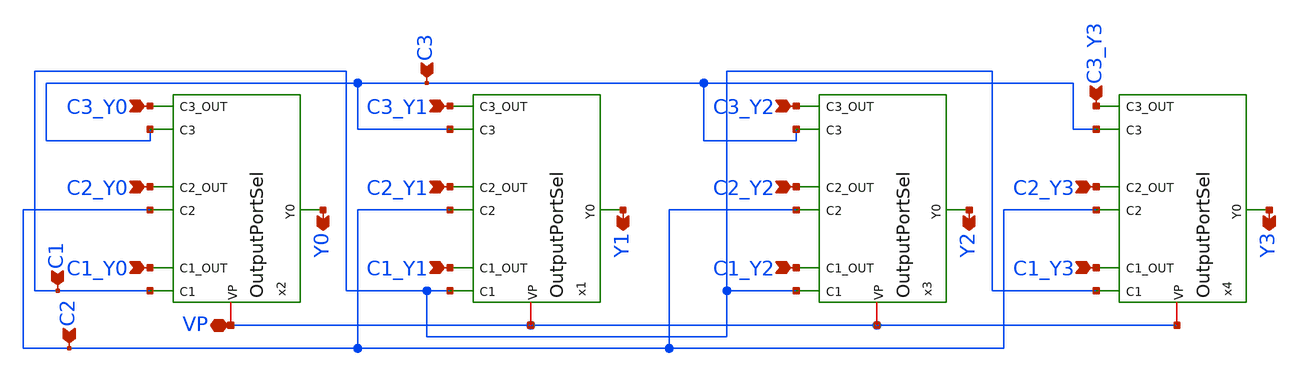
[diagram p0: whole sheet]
** sch_path: ALU_TOP_MODEL/TOPOutSel.sch
**.subckt TOPOutSel C1_Y1 VP Y0 Y1 Y2 Y3 C1_Y2 C1_Y3 C1_Y0 C2_Y0 C2_Y3 C2_Y2 C2_Y1 C3_Y0 C3_Y3 C3_Y2
*+ C3_Y1 C3 C1 C2
*.ipin C1_Y1
*.iopin VP
*.opin Y0
*.opin Y1
*.opin Y2
*.opin Y3
*.ipin C1_Y2
*.ipin C1_Y3
*.ipin C1_Y0
*.ipin C2_Y0
*.ipin C2_Y3
*.ipin C2_Y2
*.ipin C2_Y1
*.ipin C3_Y0
*.ipin C3_Y3
*.ipin C3_Y2
*.ipin C3_Y1
*.ipin C3
*.ipin C1
*.ipin C2
x2 VP C1 C1_Y0 C2 C2_Y0 C3_Y0 Y0 C3 OutputPortSel
x1 VP C1 C1_Y1 C2 C2_Y1 C3_Y1 Y1 C3 OutputPortSel
x3 VP C1 C1_Y2 C2 C2_Y2 C3_Y2 Y2 C3 OutputPortSel
x4 VP C1 C1_Y3 C2 C2_Y3 C3_Y3 Y3 C3 OutputPortSel
**.ends

* expanding   symbol:  OutputPortSel.sym # of pins=8
** sym_path: ALU_TOP_MODEL/OutputPortSel.sym
** sch_path: ALU_TOP_MODEL/OutputPortSel.sch
.subckt OutputPortSel VP C1 C1_OUT C2 C2_OUT C3 Y0 C3_OUT
*.ipin C1
*.ipin C1_OUT
*.ipin C2
*.ipin C2_OUT
*.ipin C3
*.ipin C3_OUT
*.iopin VP
*.opin Y0
x1 net1 C1 C1_OUT VP StaticAndGate
x6 net2 C2 C2_OUT VP StaticAndGate
x7 net4 C3 C3_OUT VP StaticAndGate
x3 net1 net2 net3 VP StaticORGate
x4 net3 net4 Y0 VP StaticORGate
.ends


* expanding   symbol:
*+  /home/safal/projects/GitHub_CMOS_4bit_ALU/AllSymbols&Sch/Gates/StaticAndGate.sym # of pins=4
** sym_path: AllSymbols&Sch/Gates/StaticAndGate.sym
** sch_path: AllSymbols&Sch/Gates/StaticAndGate.sch
.subckt StaticAndGate ANDOUT AND_IN1 AND_IN2 VP
*.ipin AND_IN1
*.opin ANDOUT
*.ipin AND_IN2
*.iopin VP
XM1 net2 AND_IN2 VP VP sky130_fd_pr__pfet_01v8 L=0.15 W=1 nf=1 ad='int((1 + 1)/2) * 1 / 1 * 0.29' as='int((1 + 2)/2) * 1 / 1 * 0.29'
+ pd='2*int((1 + 1)/2) * (1 / 1 + 0.29)' ps='2*int((1 + 2)/2) * (1 / 1 + 0.29)' nrd='0.29 / 1 ' nrs='0.29 / 1 '
+ sa=0 sb=0 sd=0 mult=1 m=1
XM2 net2 AND_IN1 net1 net1 sky130_fd_pr__nfet_01v8 L=0.15 W=2 nf=1 ad='int((1 + 1)/2) * 2 / 1 * 0.29'
+ as='int((1 + 2)/2) * 2 / 1 * 0.29' pd='2*int((1 + 1)/2) * (2 / 1 + 0.29)' ps='2*int((1 + 2)/2) * (2 / 1 + 0.29)'
+ nrd='0.29 / 2 ' nrs='0.29 / 2 ' sa=0 sb=0 sd=0 mult=1 m=1
XM3 net1 AND_IN2 GND GND sky130_fd_pr__nfet_01v8 L=0.15 W=2 nf=1 ad='int((1 + 1)/2) * 2 / 1 * 0.29' as='int((1 + 2)/2) * 2 / 1 * 0.29'
+ pd='2*int((1 + 1)/2) * (2 / 1 + 0.29)' ps='2*int((1 + 2)/2) * (2 / 1 + 0.29)' nrd='0.29 / 2 ' nrs='0.29 / 2 '
+ sa=0 sb=0 sd=0 mult=1 m=1
XM4 net2 AND_IN1 VP VP sky130_fd_pr__pfet_01v8 L=0.15 W=1 nf=1 ad='int((1 + 1)/2) * 1 / 1 * 0.29' as='int((1 + 2)/2) * 1 / 1 * 0.29'
+ pd='2*int((1 + 1)/2) * (1 / 1 + 0.29)' ps='2*int((1 + 2)/2) * (1 / 1 + 0.29)' nrd='0.29 / 1 ' nrs='0.29 / 1 '
+ sa=0 sb=0 sd=0 mult=1 m=1
x1 VP ANDOUT net2 inverter
.ends


* expanding   symbol:
*+  /home/safal/projects/GitHub_CMOS_4bit_ALU/AllSymbols&Sch/Gates/StaticORGate.sym # of pins=4
** sym_path: AllSymbols&Sch/Gates/StaticORGate.sym
** sch_path: AllSymbols&Sch/Gates/StaticORGate.sch
.subckt StaticORGate OR_IN2 OR_IN1 OR_OUT VP
*.ipin OR_IN1
*.opin OR_OUT
*.ipin OR_IN2
*.iopin VP
XM1 net2 OR_IN1 net1 net1 sky130_fd_pr__pfet_01v8 L=0.15 W=8 nf=1 ad='int((1 + 1)/2) * 8 / 1 * 0.29'
+ as='int((1 + 2)/2) * 8 / 1 * 0.29' pd='2*int((1 + 1)/2) * (8 / 1 + 0.29)' ps='2*int((1 + 2)/2) * (8 / 1 + 0.29)'
+ nrd='0.29 / 8 ' nrs='0.29 / 8 ' sa=0 sb=0 sd=0 mult=1 m=1
XM2 net2 OR_IN1 GND GND sky130_fd_pr__nfet_01v8 L=0.15 W=1 nf=1 ad='int((1 + 1)/2) * 1 / 1 * 0.29' as='int((1 + 2)/2) * 1 / 1 * 0.29'
+ pd='2*int((1 + 1)/2) * (1 / 1 + 0.29)' ps='2*int((1 + 2)/2) * (1 / 1 + 0.29)' nrd='0.29 / 1 ' nrs='0.29 / 1 '
+ sa=0 sb=0 sd=0 mult=1 m=1
XM5 net1 OR_IN2 VP VP sky130_fd_pr__pfet_01v8 L=0.15 W=8 nf=1 ad='int((1 + 1)/2) * 8 / 1 * 0.29' as='int((1 + 2)/2) * 8 / 1 * 0.29'
+ pd='2*int((1 + 1)/2) * (8 / 1 + 0.29)' ps='2*int((1 + 2)/2) * (8 / 1 + 0.29)' nrd='0.29 / 8 ' nrs='0.29 / 8 '
+ sa=0 sb=0 sd=0 mult=1 m=1
XM6 net2 OR_IN2 GND GND sky130_fd_pr__nfet_01v8 L=0.15 W=1 nf=1 ad='int((1 + 1)/2) * 1 / 1 * 0.29' as='int((1 + 2)/2) * 1 / 1 * 0.29'
+ pd='2*int((1 + 1)/2) * (1 / 1 + 0.29)' ps='2*int((1 + 2)/2) * (1 / 1 + 0.29)' nrd='0.29 / 1 ' nrs='0.29 / 1 '
+ sa=0 sb=0 sd=0 mult=1 m=1
x1 VP OR_OUT net2 inverter
.ends


* expanding   symbol:
*+  /home/safal/projects/GitHub_CMOS_4bit_ALU/AllSymbols&Sch/GenericSym/inverter.sym # of pins=3
** sym_path: AllSymbols&Sch/GenericSym/inverter.sym
** sch_path: AllSymbols&Sch/GenericSym/inverter.sch
.subckt inverter VP inv_out inv_in
*.ipin inv_in
*.opin inv_out
*.iopin VP
XM1 inv_out inv_in VP VP sky130_fd_pr__pfet_01v8 L=0.15 W=2 nf=1 ad='int((1 + 1)/2) * 2 / 1 * 0.29' as='int((1 + 2)/2) * 2 / 1 * 0.29'
+ pd='2*int((1 + 1)/2) * (2 / 1 + 0.29)' ps='2*int((1 + 2)/2) * (2 / 1 + 0.29)' nrd='0.29 / 2 ' nrs='0.29 / 2 '
+ sa=0 sb=0 sd=0 mult=1 m=1
XM2 inv_out inv_in GND GND sky130_fd_pr__nfet_01v8 L=0.15 W=1 nf=1 ad='int((1 + 1)/2) * 1 / 1 * 0.29'
+ as='int((1 + 2)/2) * 1 / 1 * 0.29' pd='2*int((1 + 1)/2) * (1 / 1 + 0.29)' ps='2*int((1 + 2)/2) * (1 / 1 + 0.29)'
+ nrd='0.29 / 1 ' nrs='0.29 / 1 ' sa=0 sb=0 sd=0 mult=1 m=1
.ends

.GLOBAL GND
.end
